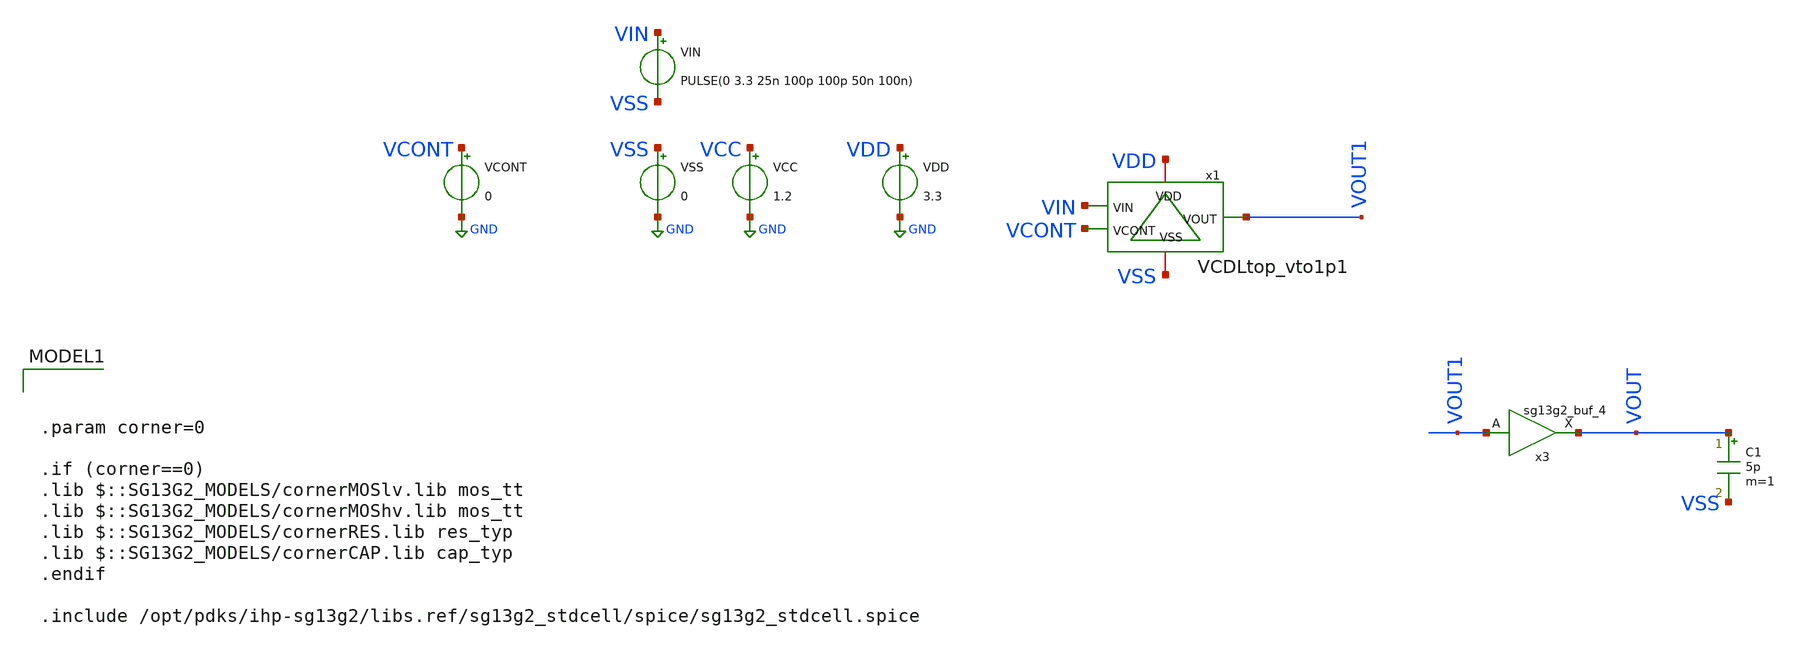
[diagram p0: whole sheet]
** sch_path: ChipUSM_AnalogTrack24/VCDL/tb_VCDL_vto1p1.sch
**.subckt tb_VCDL_vto1p1
VCC VCC GND 1.2
VSS VSS GND 0
VIN VIN VSS PULSE(0 3.3 25n 100p 100p 50n 100n)
VCONT VCONT GND 0
C1 VOUT VSS 5p m=1
VDD VDD GND 3.3
x3 VOUT VOUT1 VCC VSS sg13g2_buf_4
x1 VIN VCONT VOUT1 VSS VDD VCDLtop_vto1p1
**** begin user architecture code


.control
   save all
   compose vin_var start=0.2 stop=1.05 step=0.2
   foreach val $&vin_var
      alter vcont $val
      tran 100p 120n
   end
   plot tran1.V(VIN) tran1.V(VOUT) tran2.V(VOUT) tran3.V(VOUT) tran4.V(VOUT) tran5.V(VOUT)
   plot tran1.V(VIN) tran1.V(VOUT1) tran2.V(VOUT1) tran3.V(VOUT1) tran4.V(VOUT1) tran5.V(VOUT1)


let tdelay=vector(5)
let run=vector(5)


let run[0] = 0.2
let run[1] = 0.4
let run[2] = 0.6
let run[3] = 0.8
let run[4] = 1

meas tran tdelay[0]   TRIG tran1.V(VIN) TD=0u VAL=1.65 RISE=1  TARG tran1.V(VOUT) TD=0u VAL=0.6
+ RISE=1
meas tran tdelay[1]  TRIG tran2.V(VIN) TD=0u VAL=1.65 RISE=1  TARG tran2.V(VOUT) TD=0u VAL=0.6
+ RISE=1
meas tran tdelay[2]  TRIG tran3.V(VIN) TD=0u VAL=1.65 RISE=1  TARG tran3.V(VOUT) TD=0u VAL=0.6
+ RISE=1
meas tran tdelay[3]  TRIG tran4.V(VIN) TD=0u VAL=1.65 RISE=1  TARG tran4.V(VOUT) TD=0u VAL=0.6
+ RISE=1
meas tran tdelay[4]  TRIG tran5.V(VIN) TD=0u VAL=1.65 RISE=1  TARG tran5.V(VOUT) TD=0u VAL=0.6
+ RISE=1

setscale run
plot tdelay

.endc





.param corner=0

.if (corner==0)
.lib $::SG13G2_MODELS/cornerMOSlv.lib mos_tt
.lib $::SG13G2_MODELS/cornerMOShv.lib mos_tt
.lib $::SG13G2_MODELS/cornerRES.lib res_typ
.lib $::SG13G2_MODELS/cornerCAP.lib cap_typ
.endif

.include /opt/pdks/ihp-sg13g2/libs.ref/sg13g2_stdcell/spice/sg13g2_stdcell.spice

**** end user architecture code
**.ends
.GLOBAL GND
.end
